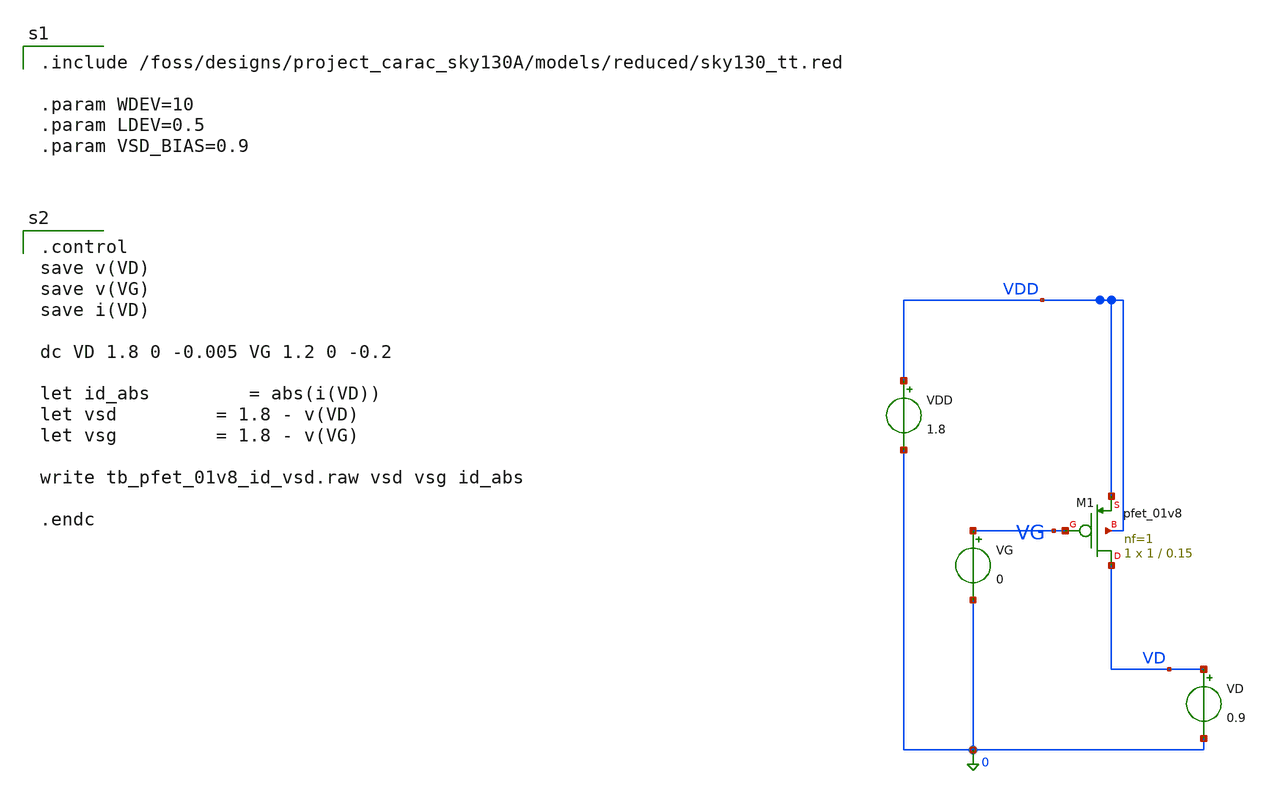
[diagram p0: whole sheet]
** sch_path: dfii/project_carac_sky130A_sim/tb_pfet_01v8_id_vsd.sch
* Copyright 2021 Stefan Frederik Schippers
* Licensed under the Apache License, Version 2.0 (the "License");
* you may not use this file except in compliance with the License.
* You may obtain a copy of the License at
* https://www.apache.org/licenses/LICENSE-2.0
* Unless required by applicable law or agreed to in writing, software
* distributed under the License is distributed on an "AS IS" BASIS,
* WITHOUT WARRANTIES OR CONDITIONS OF ANY KIND, either express or implied.
* See the License for the specific language governing permissions and
* limitations under the License.

.include /foss/designs/project_carac_sky130A/models/reduced/sky130_tt.red

.param WDEV=10
.param LDEV=0.5
.param VSD_BIAS=0.9



**.subckt tb_pfet_01v8_id_vsd
VG VG 0 0
VD VD 0 0.9
.save i(vd)
XM1 VD VG VDD VDD sky130_fd_pr__pfet_01v8 L=0.15 W=1 nf=1 ad='int((1 + 1)/2) * 1 / 1 * 0.29' as='int((1 + 2)/2) * 1 / 1 * 0.29'
+ pd='2*int((1 + 1)/2) * (1 / 1 + 0.29)' ps='2*int((1 + 2)/2) * (1 / 1 + 0.29)' nrd='0.29 / 1 ' nrs='0.29 / 1 '
+ sa=0 sb=0 sd=0 mult=1 m=1
VDD VDD 0 1.8
**.ends
**** begin user architecture code

.control
save v(VD)
save v(VG)
save i(VD)

dc VD 1.8 0 -0.005 VG 1.2 0 -0.2

let id_abs 		= abs(i(VD))
let vsd 		= 1.8 - v(VD)
let vsg 		= 1.8 - v(VG)

write tb_pfet_01v8_id_vsd.raw vsd vsg id_abs

.endc

**** end user architecture code
.end
